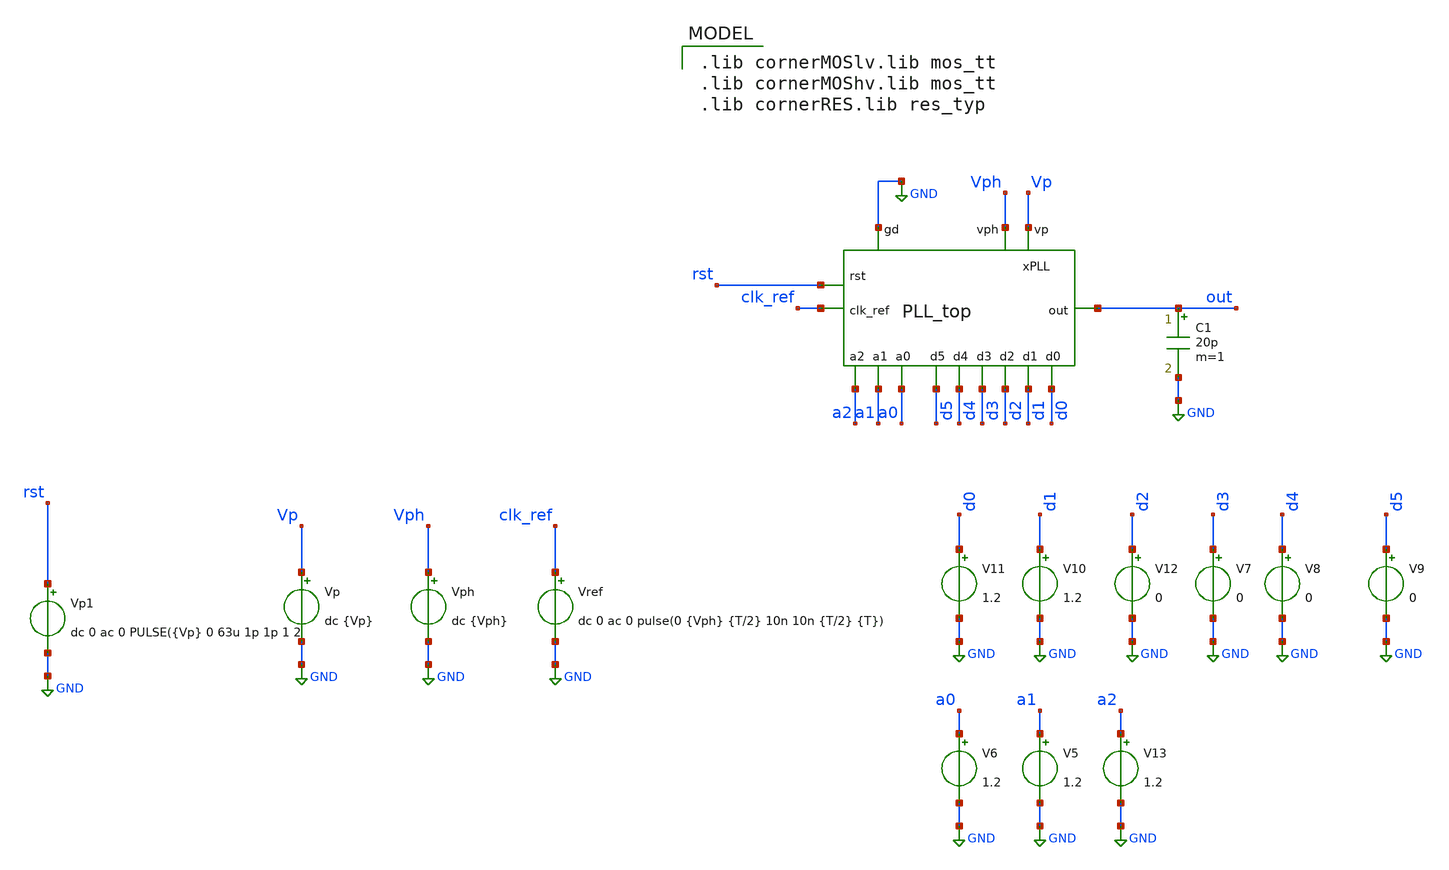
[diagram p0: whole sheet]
** sch_path: schematics/top/PLL_top_tb.sch
**.subckt PLL_top_tb
Vref clk_ref GND dc 0 ac 0 pulse(0 {Vph} {T/2} 10n 10n {T/2} {T})
Vp Vp GND dc {Vp}
Vph Vph GND dc {Vph}
C1 out GND 20p m=1
V8 d4 GND 0
V9 d5 GND 0
V11 d0 GND 1.2
V10 d1 GND 1.2
V12 d2 GND 0
V7 d3 GND 0
V5 a1 GND 1.2
V6 a0 GND 1.2
V13 a2 GND 1.2
xPLL Vp Vph GND clk_ref out d5 d3 a1 d2 d1 d0 d4 a2 a0 rst PLL_top
Vp1 rst GND dc 0 ac 0 PULSE({Vp} 0 63u 1p 1p 1 2
**** begin user architecture code
 .lib cornerMOSlv.lib mos_tt
.lib cornerMOShv.lib mos_tt
.lib cornerRES.lib res_typ




.temp=25
.param T = 31.25u

.param Vp=1.2
.param Vph=3.3
.control
save v(rst) v(out) v(xPLL.cvco) v(xPLL.cref) v(xPLL.UP) v(xPLL.DOWN) v(xPLL.vout)
+ v(xPLL.vco_out_prebuff) v(xPLL.vout_aftRC) v(xPLL.vco_out_buffered) v(xPLL.out_PLL_divided) v(xPLL.pre_LS) v(xPLL.aft_LS)
tran 0.05n 312.5u

meas tran t1 WHEN v(out)=1.65 RISE=1 FROM=0.7m
meas tran t2 WHEN v(out)=1.65 RISE=2 FROM=0.7m
meas tran period PARAM='t2-t1'
meas tran freq PARAM='1/period'

write PLL_top_tb.raw
.endc


**** end user architecture code
**.ends
.GLOBAL GND
.end
